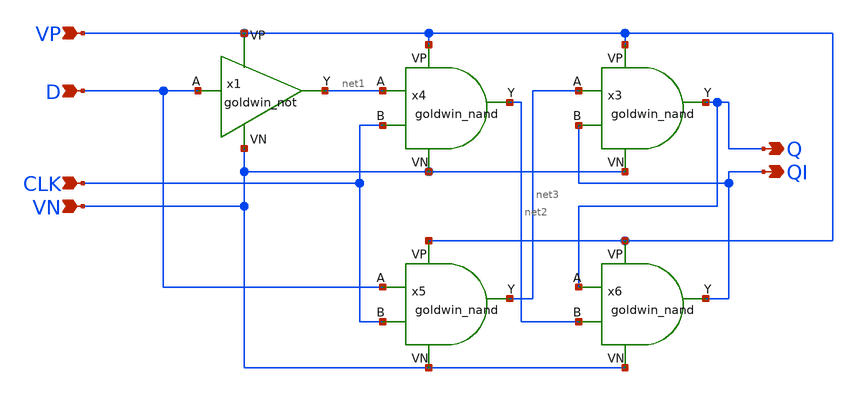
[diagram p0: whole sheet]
** sch_path: APIC-UTS/schematic/goldwin_dff/goldwin_dff.sch
**.subckt goldwin_dff D CLK VP VN Q QI
*.ipin D
*.ipin CLK
*.ipin VP
*.ipin VN
*.opin Q
*.opin QI
x1 D net1 VP VN goldwin_not
x3 net3 QI Q VP VN goldwin_nand
x4 net1 CLK net2 VP VN goldwin_nand
x5 D CLK net3 VP VN goldwin_nand
x6 Q net2 QI VP VN goldwin_nand
**.ends
.end
